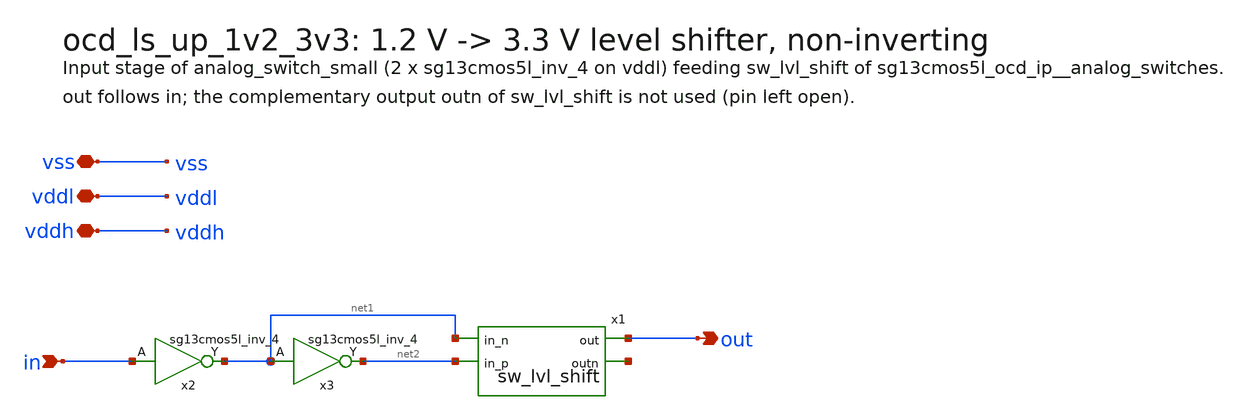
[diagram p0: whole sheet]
** sch_path: macros/ocd_ls_up_1v2_3v3/schematic/xschem/ocd_ls_up_1v2_3v3.sch
**.subckt ocd_ls_up_1v2_3v3 vss vddl vddh out in
*.iopin vss
*.iopin vddl
*.iopin vddh
*.opin out
*.ipin in
x2 net1 in vddl vss sg13cmos5l_inv_4
x3 net2 net1 vddl vss sg13cmos5l_inv_4
x1 net2 net1 out net3 vddh vss sw_lvl_shift
**.ends

* expanding   symbol:  sw_lvl_shift.sym # of pins=4
** sym_path: macros/ocd_analog_switches/schematic/xschem/sw_lvl_shift.sym
** sch_path: macros/ocd_analog_switches/schematic/xschem/sw_lvl_shift.sch
.subckt sw_lvl_shift in_p in_n out outn avdd avss
*.ipin in_n
*.ipin in_p
*.opin out
*.opin outn
XM1 net1 in_p avss avss sg13_hv_nmos w=2u l=0.5u ng=1 m=1 mm_ok=1
XM2 net1 S1_N avdd avdd sg13_hv_pmos w=0.5u l=0.5u ng=1 m=1 mm_ok=1
XM3 S1_N in_n avss avss sg13_hv_nmos w=2u l=0.5u ng=1 m=1 mm_ok=1
XM4 S1_N net1 avdd avdd sg13_hv_pmos w=0.5u l=0.5u ng=1 m=1 mm_ok=1
XM5 outn S1_N avdd avdd sg13_hv_pmos w=2u l=0.5u ng=1 m=2 mm_ok=1
XM6 outn S1_N avss avss sg13_hv_nmos w=1u l=0.5u ng=1 m=2 mm_ok=1
XM7 out outn avdd avdd sg13_hv_pmos w=2u l=0.5u ng=1 m=2 mm_ok=1
XM8 out outn avss avss sg13_hv_nmos w=1u l=0.5u ng=1 m=2 mm_ok=1
.ends

.end
